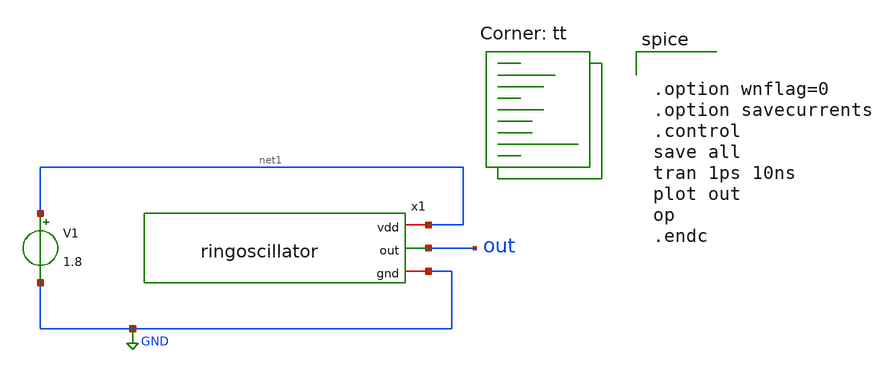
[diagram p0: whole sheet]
** sch_path: icdec_ringoscillator/ringoscillator_tb.sch
**.subckt ringoscillator_tb
x1 net1 out GND ringoscillator
V1 net1 GND 1.8
**** begin user architecture code


.option wnflag=0
.option savecurrents
.control
save all
tran 1ps 10ns
plot out
op
.endc


.lib $::SKYWATER_MODELS/sky130.lib.spice tt
**** end user architecture code
**.ends

* expanding   symbol:  ringoscillator.sym # of pins=3
** sym_path: icdec_ringoscillator/ringoscillator.sym
** sch_path: icdec_ringoscillator/ringoscillator.sch
.subckt ringoscillator vdd out gnd
*.iopin vdd
*.iopin gnd
*.opin out
x1 vdd out net1 gnd inverter2
x2 vdd net1 net2 gnd inverter2
x3 vdd net2 out gnd inverter2
.ends


* expanding   symbol:  /home/muhammadkhairulfattah/icdec_inverter2/inverter2.sym # of pins=4
** sym_path: icdec_inverter2/inverter2.sym
** sch_path: icdec_inverter2/inverter2.sch
.subckt inverter2 vdd in out gnd
*.opin out
*.ipin vdd
*.ipin in
*.ipin gnd
XM1 out in gnd gnd sky130_fd_pr__nfet_01v8 L=0.15 W=1 nf=1 ad='int((nf+1)/2) * W/nf * 0.29' as='int((nf+2)/2) * W/nf * 0.29'
+ pd='2*int((nf+1)/2) * (W/nf + 0.29)' ps='2*int((nf+2)/2) * (W/nf + 0.29)' nrd='0.29 / W' nrs='0.29 / W'
+ sa=0 sb=0 sd=0 mult=1 m=1
XM2 out in vdd vdd sky130_fd_pr__pfet_01v8 L=0.15 W=1 nf=1 ad='int((nf+1)/2) * W/nf * 0.29' as='int((nf+2)/2) * W/nf * 0.29'
+ pd='2*int((nf+1)/2) * (W/nf + 0.29)' ps='2*int((nf+2)/2) * (W/nf + 0.29)' nrd='0.29 / W' nrs='0.29 / W'
+ sa=0 sb=0 sd=0 mult=1 m=1
.ends

.GLOBAL GND
.end
